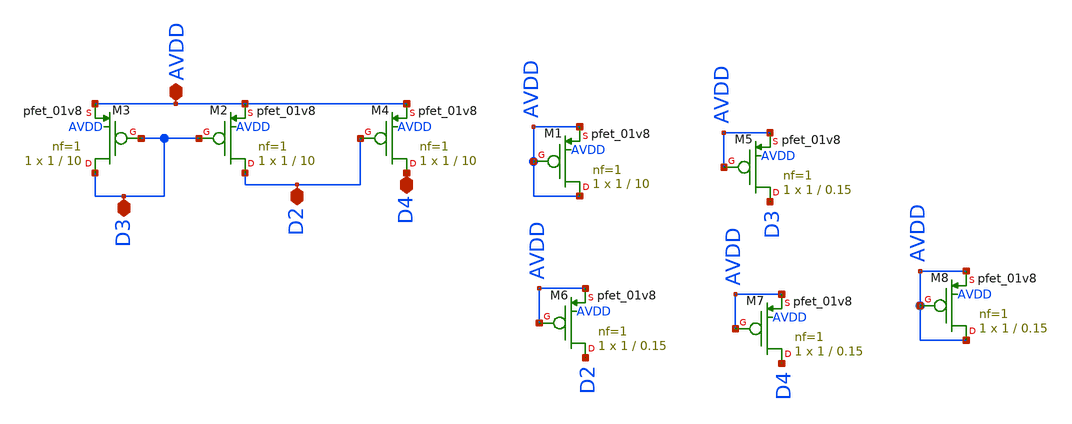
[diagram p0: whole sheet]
** sch_path: magic/pmos_startup.sch
**.subckt pmos_startup AVDD D2 D3 D4
*.iopin AVDD
*.iopin D2
*.iopin D3
*.iopin D4
XM2 D2 D3 AVDD AVDD sky130_fd_pr__pfet_01v8 L=10 W=1 nf=1 ad='int((nf+1)/2) * W/nf * 0.29' as='int((nf+2)/2) * W/nf * 0.29'
+ pd='2*int((nf+1)/2) * (W/nf + 0.29)' ps='2*int((nf+2)/2) * (W/nf + 0.29)' nrd='0.29 / W' nrs='0.29 / W'
+ sa=0 sb=0 sd=0 mult=1 m=1
XM3 D3 D3 AVDD AVDD sky130_fd_pr__pfet_01v8 L=10 W=1 nf=1 ad='int((nf+1)/2) * W/nf * 0.29' as='int((nf+2)/2) * W/nf * 0.29'
+ pd='2*int((nf+1)/2) * (W/nf + 0.29)' ps='2*int((nf+2)/2) * (W/nf + 0.29)' nrd='0.29 / W' nrs='0.29 / W'
+ sa=0 sb=0 sd=0 mult=1 m=1
XM4 D4 D2 AVDD AVDD sky130_fd_pr__pfet_01v8 L=10 W=1 nf=1 ad='int((nf+1)/2) * W/nf * 0.29' as='int((nf+2)/2) * W/nf * 0.29'
+ pd='2*int((nf+1)/2) * (W/nf + 0.29)' ps='2*int((nf+2)/2) * (W/nf + 0.29)' nrd='0.29 / W' nrs='0.29 / W'
+ sa=0 sb=0 sd=0 mult=1 m=1
XM1 AVDD AVDD AVDD AVDD sky130_fd_pr__pfet_01v8 L=10 W=1 nf=1 ad='int((nf+1)/2) * W/nf * 0.29' as='int((nf+2)/2) * W/nf * 0.29'
+ pd='2*int((nf+1)/2) * (W/nf + 0.29)' ps='2*int((nf+2)/2) * (W/nf + 0.29)' nrd='0.29 / W' nrs='0.29 / W'
+ sa=0 sb=0 sd=0 mult=1 m=1
XM5 D3 AVDD AVDD AVDD sky130_fd_pr__pfet_01v8 L=0.15 W=1 nf=1 ad='int((nf+1)/2) * W/nf * 0.29' as='int((nf+2)/2) * W/nf * 0.29'
+ pd='2*int((nf+1)/2) * (W/nf + 0.29)' ps='2*int((nf+2)/2) * (W/nf + 0.29)' nrd='0.29 / W' nrs='0.29 / W'
+ sa=0 sb=0 sd=0 mult=1 m=1
XM6 D2 AVDD AVDD AVDD sky130_fd_pr__pfet_01v8 L=0.15 W=1 nf=1 ad='int((nf+1)/2) * W/nf * 0.29' as='int((nf+2)/2) * W/nf * 0.29'
+ pd='2*int((nf+1)/2) * (W/nf + 0.29)' ps='2*int((nf+2)/2) * (W/nf + 0.29)' nrd='0.29 / W' nrs='0.29 / W'
+ sa=0 sb=0 sd=0 mult=1 m=1
XM7 D4 AVDD AVDD AVDD sky130_fd_pr__pfet_01v8 L=0.15 W=1 nf=1 ad='int((nf+1)/2) * W/nf * 0.29' as='int((nf+2)/2) * W/nf * 0.29'
+ pd='2*int((nf+1)/2) * (W/nf + 0.29)' ps='2*int((nf+2)/2) * (W/nf + 0.29)' nrd='0.29 / W' nrs='0.29 / W'
+ sa=0 sb=0 sd=0 mult=1 m=1
XM8 AVDD AVDD AVDD AVDD sky130_fd_pr__pfet_01v8 L=0.15 W=1 nf=1 ad='int((nf+1)/2) * W/nf * 0.29' as='int((nf+2)/2) * W/nf * 0.29'
+ pd='2*int((nf+1)/2) * (W/nf + 0.29)' ps='2*int((nf+2)/2) * (W/nf + 0.29)' nrd='0.29 / W' nrs='0.29 / W'
+ sa=0 sb=0 sd=0 mult=1 m=1
**.ends
.end
